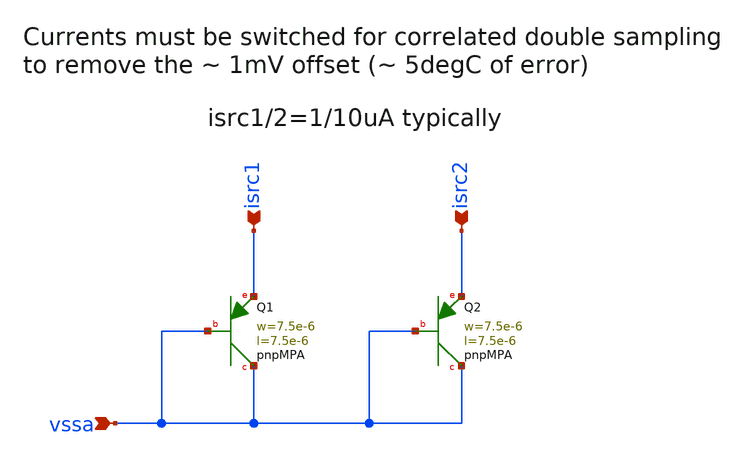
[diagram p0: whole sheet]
** sch_path: Schematics_Layout/sunrise_tsns_PNP/sunrise_tsns_PNP.sch
**.subckt sunrise_tsns_PNP isrc1 isrc2 vssa
*.ipin isrc1
*.ipin isrc2
*.ipin vssa
XQ2 vssa vssa isrc2 pnpMPA a=56.25p p=30u m=50
XQ1 vssa vssa isrc1 pnpMPA a=56.25p p=30u m=50
**.ends
.end
